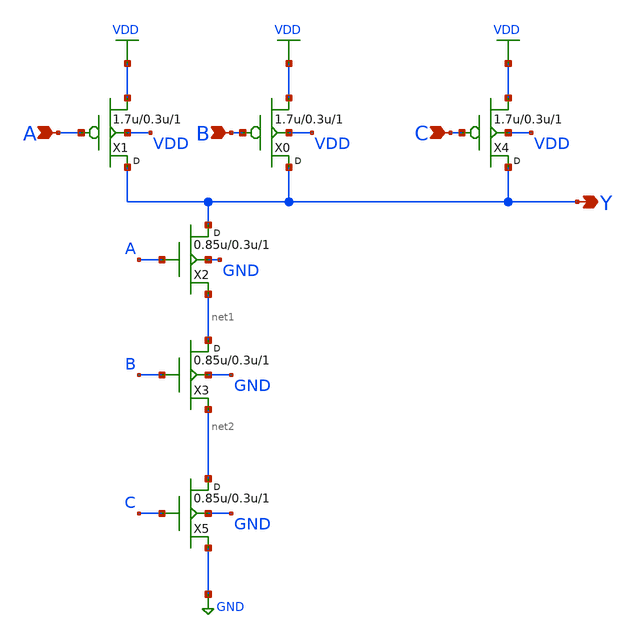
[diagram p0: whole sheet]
** sch_path: designs/libs/core_digital/gf180mcu_osu_sc_gp12t3v3/cells/nand3/gf180mcu_osu_sc_gp12t3v3__nand3_1.sch
**.subckt gf180mcu_osu_sc_gp12t3v3__nand3_1 A B Y C
*.ipin A
*.ipin B
*.opin Y
*.ipin C
X1 Y A VDD VDD pfet_03p3 w=1.7u l=0.3u m=1
X0 Y B VDD VDD pfet_03p3 w=1.7u l=0.3u m=1
X2 Y A net1 GND nfet_03p3 w=0.85u l=0.3u m=1
X3 net1 B net2 GND nfet_03p3 w=0.85u l=0.3u m=1
X4 Y C VDD VDD pfet_03p3 w=1.7u l=0.3u m=1
X5 net2 C GND GND nfet_03p3 w=0.85u l=0.3u m=1
**.ends
.GLOBAL VDD
.GLOBAL GND
.end
